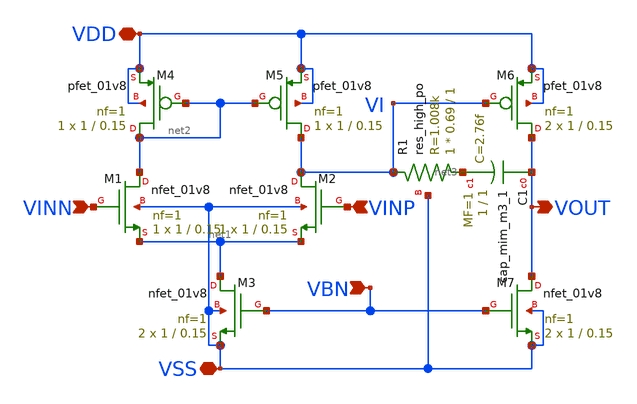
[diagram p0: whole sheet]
** sch_path: analog/bootcamp_opamp/schematics/bootcamp_opamp.sch
**.subckt bootcamp_opamp VINN VDD VSS VINP VOUT VBN
*.ipin VINN
*.iopin VDD
*.iopin VSS
*.ipin VINP
*.opin VOUT
*.ipin VBN
XM1 net2 VINN net1 VSS sky130_fd_pr__nfet_01v8 L=0.15 W=1 nf=1 ad='int((nf+1)/2) * W/nf * 0.29' as='int((nf+2)/2) * W/nf * 0.29'
+ pd='2*int((nf+1)/2) * (W/nf + 0.29)' ps='2*int((nf+2)/2) * (W/nf + 0.29)' nrd='0.29 / W' nrs='0.29 / W'
+ sa=0 sb=0 sd=0 mult=1 m=1
XM2 VI VINP net1 VSS sky130_fd_pr__nfet_01v8 L=0.15 W=1 nf=1 ad='int((nf+1)/2) * W/nf * 0.29' as='int((nf+2)/2) * W/nf * 0.29'
+ pd='2*int((nf+1)/2) * (W/nf + 0.29)' ps='2*int((nf+2)/2) * (W/nf + 0.29)' nrd='0.29 / W' nrs='0.29 / W'
+ sa=0 sb=0 sd=0 mult=1 m=1
XM3 net1 VBN VSS VSS sky130_fd_pr__nfet_01v8 L=0.15 W=1 nf=1 ad='int((nf+1)/2) * W/nf * 0.29' as='int((nf+2)/2) * W/nf * 0.29'
+ pd='2*int((nf+1)/2) * (W/nf + 0.29)' ps='2*int((nf+2)/2) * (W/nf + 0.29)' nrd='0.29 / W' nrs='0.29 / W'
+ sa=0 sb=0 sd=0 mult=2 m=2
XM7 VOUT VBN VSS VSS sky130_fd_pr__nfet_01v8 L=0.15 W=1 nf=1 ad='int((nf+1)/2) * W/nf * 0.29' as='int((nf+2)/2) * W/nf * 0.29'
+ pd='2*int((nf+1)/2) * (W/nf + 0.29)' ps='2*int((nf+2)/2) * (W/nf + 0.29)' nrd='0.29 / W' nrs='0.29 / W'
+ sa=0 sb=0 sd=0 mult=2 m=2
XM4 net2 net2 VDD VDD sky130_fd_pr__pfet_01v8 L=0.15 W=1 nf=1 ad='int((nf+1)/2) * W/nf * 0.29' as='int((nf+2)/2) * W/nf * 0.29'
+ pd='2*int((nf+1)/2) * (W/nf + 0.29)' ps='2*int((nf+2)/2) * (W/nf + 0.29)' nrd='0.29 / W' nrs='0.29 / W'
+ sa=0 sb=0 sd=0 mult=1 m=1
XM5 VI net2 VDD VDD sky130_fd_pr__pfet_01v8 L=0.15 W=1 nf=1 ad='int((nf+1)/2) * W/nf * 0.29' as='int((nf+2)/2) * W/nf * 0.29'
+ pd='2*int((nf+1)/2) * (W/nf + 0.29)' ps='2*int((nf+2)/2) * (W/nf + 0.29)' nrd='0.29 / W' nrs='0.29 / W'
+ sa=0 sb=0 sd=0 mult=1 m=1
XM6 VOUT VI VDD VDD sky130_fd_pr__pfet_01v8 L=0.15 W=1 nf=1 ad='int((nf+1)/2) * W/nf * 0.29' as='int((nf+2)/2) * W/nf * 0.29'
+ pd='2*int((nf+1)/2) * (W/nf + 0.29)' ps='2*int((nf+2)/2) * (W/nf + 0.29)' nrd='0.29 / W' nrs='0.29 / W'
+ sa=0 sb=0 sd=0 mult=2 m=2
XR1 net3 VI VSS sky130_fd_pr__res_high_po W=0.69 L=1 mult=1 m=1
XC1 VOUT net3 sky130_fd_pr__cap_mim_m3_1 W=1 L=1 MF=1 m=1
**.ends
.end
